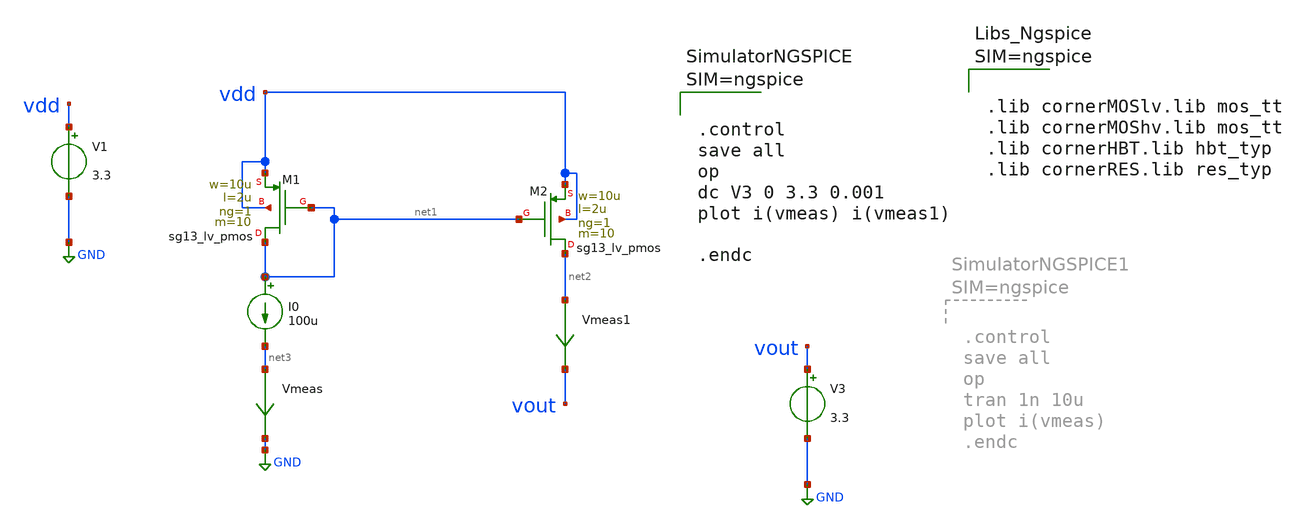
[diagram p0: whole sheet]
** sch_path: Schematics/pmos_current.sch
**.subckt pmos_current
I0 net1 net3 100u
V1 vdd GND 3.3
V3 vout GND 3.3
Vmeas net3 GND 0
.save i(vmeas)
Vmeas1 net2 vout 0
.save i(vmeas1)
XM2 net2 net1 vdd vdd sg13_lv_pmos w=10u l=2u ng=1 m=10 mm_ok=1
XM1 net1 net1 vdd vdd sg13_lv_pmos w=10u l=2u ng=1 m=10 mm_ok=1
**** begin user architecture code



.control
save all
op
dc V3 0 3.3 0.001
plot i(vmeas) i(vmeas1)

.endc






.lib cornerMOSlv.lib mos_tt
.lib cornerMOShv.lib mos_tt
.lib cornerHBT.lib hbt_typ
.lib cornerRES.lib res_typ



**** end user architecture code
**.ends
.GLOBAL GND
.end
